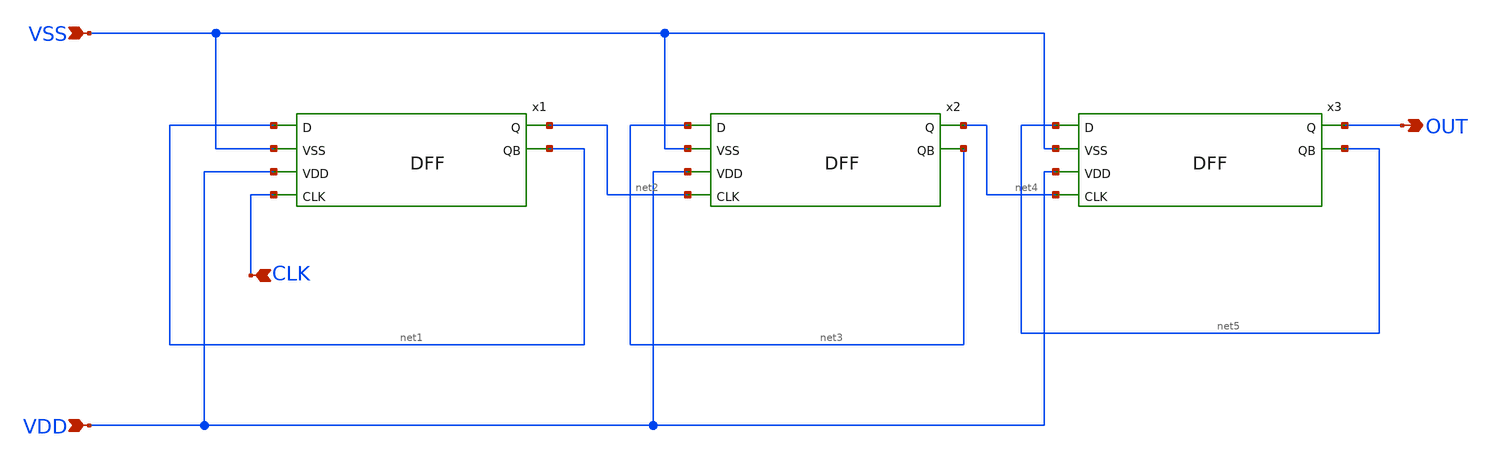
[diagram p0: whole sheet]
** sch_path: designs/libs/tb_analog/tb_frquency_divider/Frequency_Divider.sch
**.subckt Frequency_Divider VSS VDD CLK OUT
*.ipin VSS
*.ipin VDD
*.ipin CLK
*.opin OUT
x1 net1 VSS VDD net2 CLK net1 DFF
x2 net3 VSS VDD net4 net2 net3 DFF
x3 net5 VSS VDD OUT net4 net5 DFF
**.ends
.end
